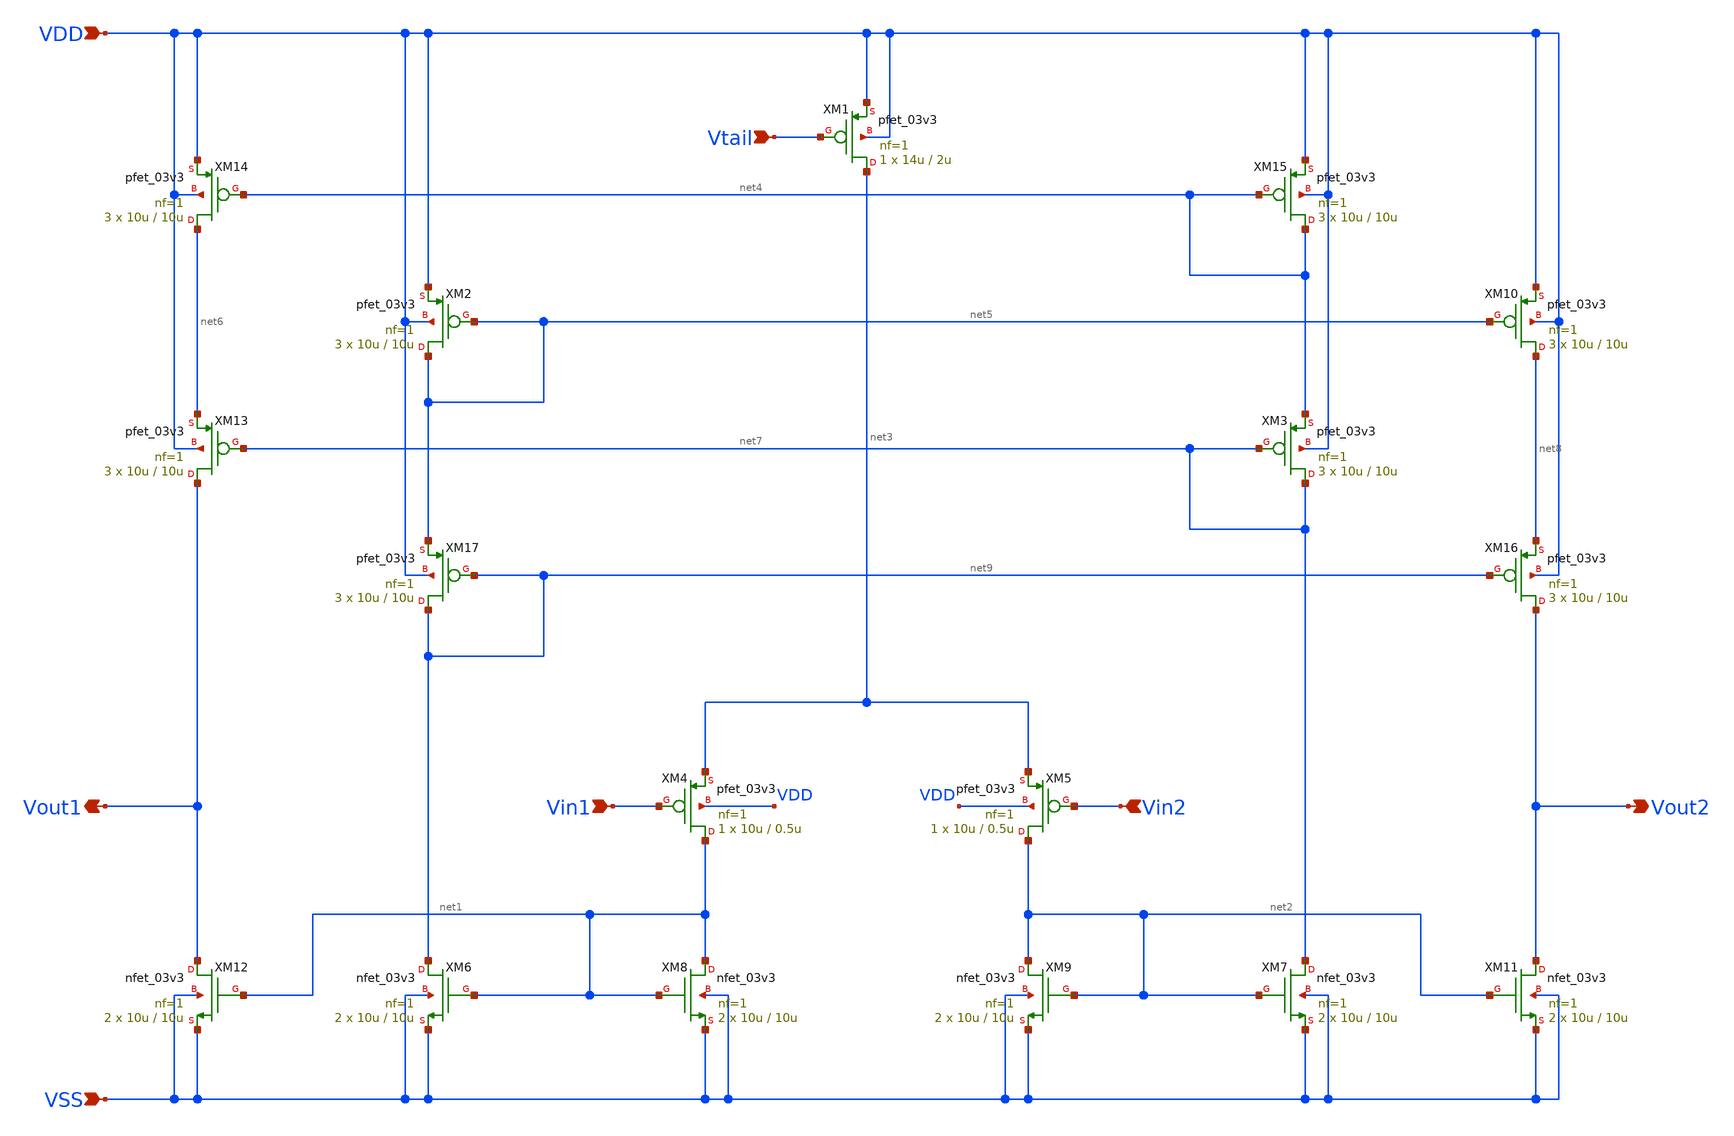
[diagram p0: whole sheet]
** sch_path: designs/libs/core_ina/ina_ota/ina_ota_2.sch
**.subckt ina_ota_2 Vin1 Vin2 Vtail VSS Vout2 VDD Vout1
*.ipin Vin1
*.ipin Vin2
*.ipin Vtail
*.ipin VSS
*.opin Vout2
*.ipin VDD
*.opin Vout1
XM2 net5 net5 VDD VDD pfet_03v3 L=10u W=10u nf=1 ad='int((nf+1)/2) * W/nf * 0.18u' as='int((nf+2)/2) * W/nf * 0.18u'
+ pd='2*int((nf+1)/2) * (W/nf + 0.18u)' ps='2*int((nf+2)/2) * (W/nf + 0.18u)' nrd='0.18u / W' nrs='0.18u / W'
+ sa=0 sb=0 sd=0 m=3
XM1 net3 Vtail VDD VDD pfet_03v3 L=2u W=14u nf=1 ad='int((nf+1)/2) * W/nf * 0.18u' as='int((nf+2)/2) * W/nf * 0.18u'
+ pd='2*int((nf+1)/2) * (W/nf + 0.18u)' ps='2*int((nf+2)/2) * (W/nf + 0.18u)' nrd='0.18u / W' nrs='0.18u / W'
+ sa=0 sb=0 sd=0 m=1
XM3 net7 net7 net4 VDD pfet_03v3 L=10u W=10u nf=1 ad='int((nf+1)/2) * W/nf * 0.18u' as='int((nf+2)/2) * W/nf * 0.18u'
+ pd='2*int((nf+1)/2) * (W/nf + 0.18u)' ps='2*int((nf+2)/2) * (W/nf + 0.18u)' nrd='0.18u / W' nrs='0.18u / W'
+ sa=0 sb=0 sd=0 m=3
XM4 net1 Vin1 net3 VDD pfet_03v3 L=0.5u W=10u nf=1 ad='int((nf+1)/2) * W/nf * 0.18u' as='int((nf+2)/2) * W/nf * 0.18u'
+ pd='2*int((nf+1)/2) * (W/nf + 0.18u)' ps='2*int((nf+2)/2) * (W/nf + 0.18u)' nrd='0.18u / W' nrs='0.18u / W'
+ sa=0 sb=0 sd=0 m=1
XM5 net2 Vin2 net3 VDD pfet_03v3 L=0.5u W=10u nf=1 ad='int((nf+1)/2) * W/nf * 0.18u' as='int((nf+2)/2) * W/nf * 0.18u'
+ pd='2*int((nf+1)/2) * (W/nf + 0.18u)' ps='2*int((nf+2)/2) * (W/nf + 0.18u)' nrd='0.18u / W' nrs='0.18u / W'
+ sa=0 sb=0 sd=0 m=1
XM6 net9 net1 VSS VSS nfet_03v3 L=10u W=10u nf=1 ad='int((nf+1)/2) * W/nf * 0.18u' as='int((nf+2)/2) * W/nf * 0.18u'
+ pd='2*int((nf+1)/2) * (W/nf + 0.18u)' ps='2*int((nf+2)/2) * (W/nf + 0.18u)' nrd='0.18u / W' nrs='0.18u / W'
+ sa=0 sb=0 sd=0 m=2
XM7 net7 net2 VSS VSS nfet_03v3 L=10u W=10u nf=1 ad='int((nf+1)/2) * W/nf * 0.18u' as='int((nf+2)/2) * W/nf * 0.18u'
+ pd='2*int((nf+1)/2) * (W/nf + 0.18u)' ps='2*int((nf+2)/2) * (W/nf + 0.18u)' nrd='0.18u / W' nrs='0.18u / W'
+ sa=0 sb=0 sd=0 m=2
XM8 net1 net1 VSS VSS nfet_03v3 L=10u W=10u nf=1 ad='int((nf+1)/2) * W/nf * 0.18u' as='int((nf+2)/2) * W/nf * 0.18u'
+ pd='2*int((nf+1)/2) * (W/nf + 0.18u)' ps='2*int((nf+2)/2) * (W/nf + 0.18u)' nrd='0.18u / W' nrs='0.18u / W'
+ sa=0 sb=0 sd=0 m=2
XM9 net2 net2 VSS VSS nfet_03v3 L=10u W=10u nf=1 ad='int((nf+1)/2) * W/nf * 0.18u' as='int((nf+2)/2) * W/nf * 0.18u'
+ pd='2*int((nf+1)/2) * (W/nf + 0.18u)' ps='2*int((nf+2)/2) * (W/nf + 0.18u)' nrd='0.18u / W' nrs='0.18u / W'
+ sa=0 sb=0 sd=0 m=2
XM10 net8 net5 VDD VDD pfet_03v3 L=10u W=10u nf=1 ad='int((nf+1)/2) * W/nf * 0.18u' as='int((nf+2)/2) * W/nf * 0.18u'
+ pd='2*int((nf+1)/2) * (W/nf + 0.18u)' ps='2*int((nf+2)/2) * (W/nf + 0.18u)' nrd='0.18u / W' nrs='0.18u / W'
+ sa=0 sb=0 sd=0 m=3
XM11 Vout2 net2 VSS VSS nfet_03v3 L=10u W=10u nf=1 ad='int((nf+1)/2) * W/nf * 0.18u' as='int((nf+2)/2) * W/nf * 0.18u'
+ pd='2*int((nf+1)/2) * (W/nf + 0.18u)' ps='2*int((nf+2)/2) * (W/nf + 0.18u)' nrd='0.18u / W' nrs='0.18u / W'
+ sa=0 sb=0 sd=0 m=2
XM12 Vout1 net1 VSS VSS nfet_03v3 L=10u W=10u nf=1 ad='int((nf+1)/2) * W/nf * 0.18u' as='int((nf+2)/2) * W/nf * 0.18u'
+ pd='2*int((nf+1)/2) * (W/nf + 0.18u)' ps='2*int((nf+2)/2) * (W/nf + 0.18u)' nrd='0.18u / W' nrs='0.18u / W'
+ sa=0 sb=0 sd=0 m=2
XM13 Vout1 net7 net6 VDD pfet_03v3 L=10u W=10u nf=1 ad='int((nf+1)/2) * W/nf * 0.18u' as='int((nf+2)/2) * W/nf * 0.18u'
+ pd='2*int((nf+1)/2) * (W/nf + 0.18u)' ps='2*int((nf+2)/2) * (W/nf + 0.18u)' nrd='0.18u / W' nrs='0.18u / W'
+ sa=0 sb=0 sd=0 m=3
XM14 net6 net4 VDD VDD pfet_03v3 L=10u W=10u nf=1 ad='int((nf+1)/2) * W/nf * 0.18u' as='int((nf+2)/2) * W/nf * 0.18u'
+ pd='2*int((nf+1)/2) * (W/nf + 0.18u)' ps='2*int((nf+2)/2) * (W/nf + 0.18u)' nrd='0.18u / W' nrs='0.18u / W'
+ sa=0 sb=0 sd=0 m=3
XM15 net4 net4 VDD VDD pfet_03v3 L=10u W=10u nf=1 ad='int((nf+1)/2) * W/nf * 0.18u' as='int((nf+2)/2) * W/nf * 0.18u'
+ pd='2*int((nf+1)/2) * (W/nf + 0.18u)' ps='2*int((nf+2)/2) * (W/nf + 0.18u)' nrd='0.18u / W' nrs='0.18u / W'
+ sa=0 sb=0 sd=0 m=3
XM16 Vout2 net9 net8 VDD pfet_03v3 L=10u W=10u nf=1 ad='int((nf+1)/2) * W/nf * 0.18u' as='int((nf+2)/2) * W/nf * 0.18u'
+ pd='2*int((nf+1)/2) * (W/nf + 0.18u)' ps='2*int((nf+2)/2) * (W/nf + 0.18u)' nrd='0.18u / W' nrs='0.18u / W'
+ sa=0 sb=0 sd=0 m=3
XM17 net9 net9 net5 VDD pfet_03v3 L=10u W=10u nf=1 ad='int((nf+1)/2) * W/nf * 0.18u' as='int((nf+2)/2) * W/nf * 0.18u'
+ pd='2*int((nf+1)/2) * (W/nf + 0.18u)' ps='2*int((nf+2)/2) * (W/nf + 0.18u)' nrd='0.18u / W' nrs='0.18u / W'
+ sa=0 sb=0 sd=0 m=3
**.ends
.end
